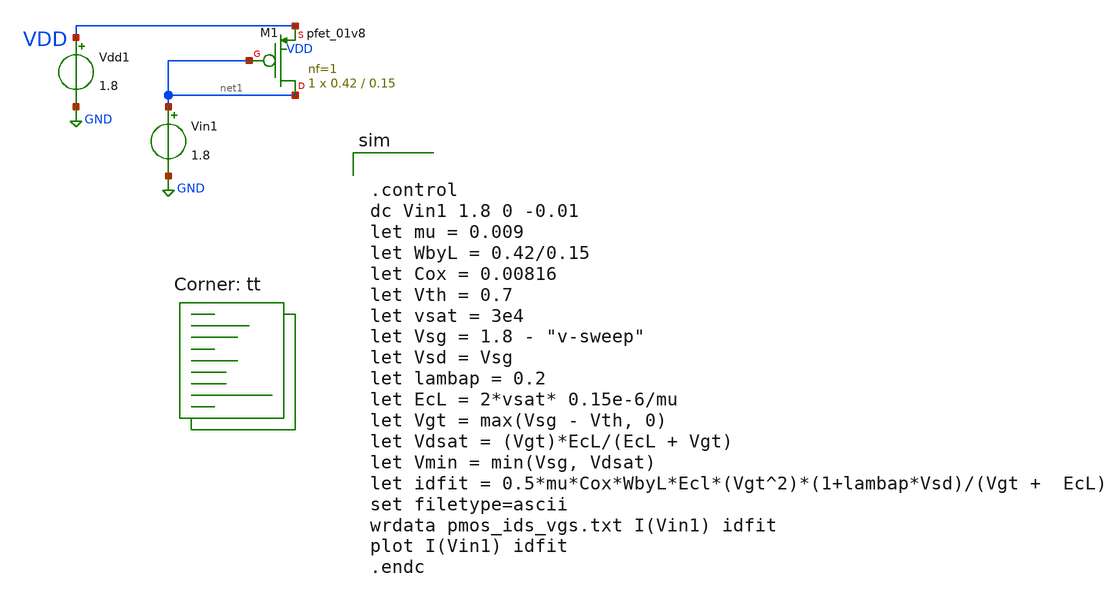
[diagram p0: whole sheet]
** sch_path: tutorial_2/tutorial_2_2a.sch
**.subckt tutorial_2_2a
XM1 net1 net1 VDD VDD sky130_fd_pr__pfet_01v8 L=0.15 W=0.42 nf=1 ad='int((nf+1)/2) * W/nf * 0.29' as='int((nf+2)/2) * W/nf * 0.29'
+ pd='2*int((nf+1)/2) * (W/nf + 0.29)' ps='2*int((nf+2)/2) * (W/nf + 0.29)' nrd='0.29 / W' nrs='0.29 / W'
+ sa=0 sb=0 sd=0 mult=1 m=1
Vdd1 VDD GND 1.8
Vin1 net1 GND 1.8
**** begin user architecture code


.control
dc Vin1 1.8 0 -0.01
let mu = 0.009
let WbyL = 0.42/0.15
let Cox = 0.00816
let Vth = 0.7
let vsat = 3e4
let Vsg = 1.8 - "v-sweep"
let Vsd = Vsg
let lambap = 0.2
let EcL = 2*vsat* 0.15e-6/mu
let Vgt = max(Vsg - Vth, 0)
let Vdsat = (Vgt)*EcL/(EcL + Vgt)
let Vmin = min(Vsg, Vdsat)
let idfit = 0.5*mu*Cox*WbyL*Ecl*(Vgt^2)*(1+lambap*Vsd)/(Vgt +  EcL)
set filetype=ascii
wrdata pmos_ids_vgs.txt I(Vin1) idfit
plot I(Vin1) idfit
.endc

.lib $::SKYWATER_MODELS/sky130.lib.spice tt
**** end user architecture code
**.ends
.GLOBAL GND
.end
